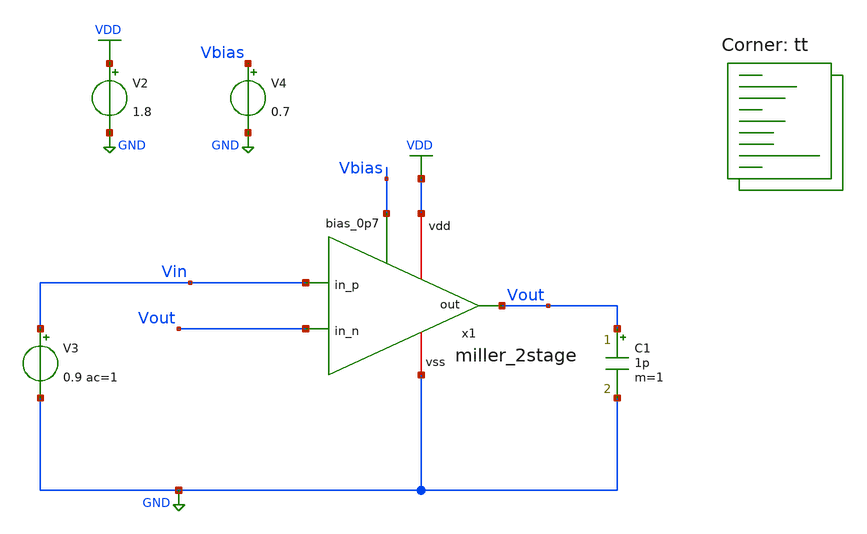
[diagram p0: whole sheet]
** sch_path: xschem/cmos_imager/tb_unity_gain_buffer.sch
**.subckt tb_unity_gain_buffer
V3 Vin GND 0.9 ac=1
C1 Vout GND 1p m=1
V4 Vbias GND 0.7
x1 VDD Vout Vin Vout Vbias GND miller_2stage
V2 VDD GND 1.8
**** begin user architecture code


.param temp=27

.op
.ac dec 10 1 1G
*.tran 0.001 50n 20n

.control
ac dec 10 1 1G
let phase = 180/PI*vp(Vout)

plot vdb(Vout) phase
plot phase

.endc

.save all



.lib $::SKYWATER_MODELS/sky130.lib.spice tt
**** end user architecture code
**.ends
.GLOBAL GND
.GLOBAL VDD
.end
